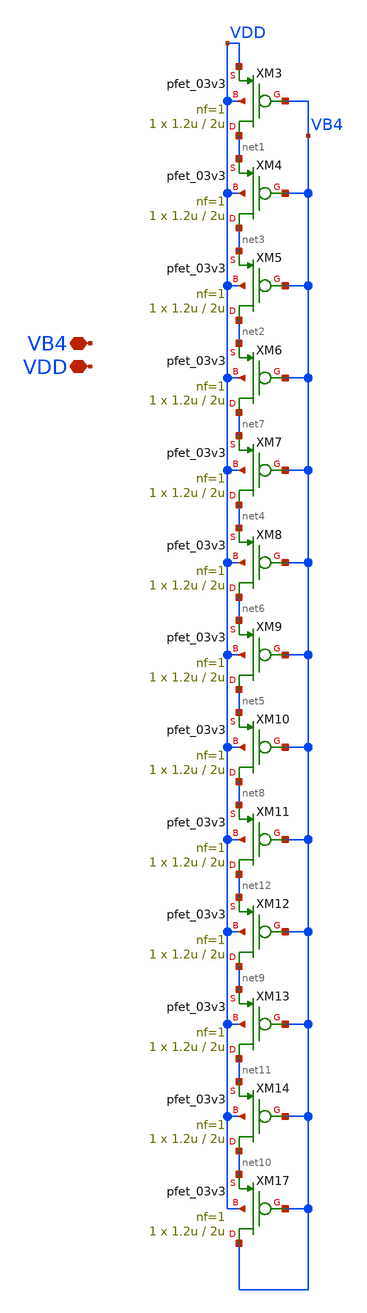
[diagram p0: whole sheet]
** sch_path: TIA_Filter/Folded/FC_bias_vb4.sch
**.subckt FC_bias_vb4 VDD VB4
*.iopin VDD
*.iopin VB4
XM3 net1 VB4 VDD VDD pfet_03v3 L=2u W=1.2u nf=1 ad='int((nf+1)/2) * W/nf * 0.18u' as='int((nf+2)/2) * W/nf * 0.18u'
+ pd='2*int((nf+1)/2) * (W/nf + 0.18u)' ps='2*int((nf+2)/2) * (W/nf + 0.18u)' nrd='0.18u / W' nrs='0.18u / W'
+ sa=0 sb=0 sd=0 m=1
XM4 net3 VB4 net1 VDD pfet_03v3 L=2u W=1.2u nf=1 ad='int((nf+1)/2) * W/nf * 0.18u' as='int((nf+2)/2) * W/nf * 0.18u'
+ pd='2*int((nf+1)/2) * (W/nf + 0.18u)' ps='2*int((nf+2)/2) * (W/nf + 0.18u)' nrd='0.18u / W' nrs='0.18u / W'
+ sa=0 sb=0 sd=0 m=1
XM5 net2 VB4 net3 VDD pfet_03v3 L=2u W=1.2u nf=1 ad='int((nf+1)/2) * W/nf * 0.18u' as='int((nf+2)/2) * W/nf * 0.18u'
+ pd='2*int((nf+1)/2) * (W/nf + 0.18u)' ps='2*int((nf+2)/2) * (W/nf + 0.18u)' nrd='0.18u / W' nrs='0.18u / W'
+ sa=0 sb=0 sd=0 m=1
XM6 net7 VB4 net2 VDD pfet_03v3 L=2u W=1.2u nf=1 ad='int((nf+1)/2) * W/nf * 0.18u' as='int((nf+2)/2) * W/nf * 0.18u'
+ pd='2*int((nf+1)/2) * (W/nf + 0.18u)' ps='2*int((nf+2)/2) * (W/nf + 0.18u)' nrd='0.18u / W' nrs='0.18u / W'
+ sa=0 sb=0 sd=0 m=1
XM7 net4 VB4 net7 VDD pfet_03v3 L=2u W=1.2u nf=1 ad='int((nf+1)/2) * W/nf * 0.18u' as='int((nf+2)/2) * W/nf * 0.18u'
+ pd='2*int((nf+1)/2) * (W/nf + 0.18u)' ps='2*int((nf+2)/2) * (W/nf + 0.18u)' nrd='0.18u / W' nrs='0.18u / W'
+ sa=0 sb=0 sd=0 m=1
XM8 net6 VB4 net4 VDD pfet_03v3 L=2u W=1.2u nf=1 ad='int((nf+1)/2) * W/nf * 0.18u' as='int((nf+2)/2) * W/nf * 0.18u'
+ pd='2*int((nf+1)/2) * (W/nf + 0.18u)' ps='2*int((nf+2)/2) * (W/nf + 0.18u)' nrd='0.18u / W' nrs='0.18u / W'
+ sa=0 sb=0 sd=0 m=1
XM9 net5 VB4 net6 VDD pfet_03v3 L=2u W=1.2u nf=1 ad='int((nf+1)/2) * W/nf * 0.18u' as='int((nf+2)/2) * W/nf * 0.18u'
+ pd='2*int((nf+1)/2) * (W/nf + 0.18u)' ps='2*int((nf+2)/2) * (W/nf + 0.18u)' nrd='0.18u / W' nrs='0.18u / W'
+ sa=0 sb=0 sd=0 m=1
XM10 net8 VB4 net5 VDD pfet_03v3 L=2u W=1.2u nf=1 ad='int((nf+1)/2) * W/nf * 0.18u' as='int((nf+2)/2) * W/nf * 0.18u'
+ pd='2*int((nf+1)/2) * (W/nf + 0.18u)' ps='2*int((nf+2)/2) * (W/nf + 0.18u)' nrd='0.18u / W' nrs='0.18u / W'
+ sa=0 sb=0 sd=0 m=1
XM11 net12 VB4 net8 VDD pfet_03v3 L=2u W=1.2u nf=1 ad='int((nf+1)/2) * W/nf * 0.18u' as='int((nf+2)/2) * W/nf * 0.18u'
+ pd='2*int((nf+1)/2) * (W/nf + 0.18u)' ps='2*int((nf+2)/2) * (W/nf + 0.18u)' nrd='0.18u / W' nrs='0.18u / W'
+ sa=0 sb=0 sd=0 m=1
XM12 net9 VB4 net12 VDD pfet_03v3 L=2u W=1.2u nf=1 ad='int((nf+1)/2) * W/nf * 0.18u' as='int((nf+2)/2) * W/nf * 0.18u'
+ pd='2*int((nf+1)/2) * (W/nf + 0.18u)' ps='2*int((nf+2)/2) * (W/nf + 0.18u)' nrd='0.18u / W' nrs='0.18u / W'
+ sa=0 sb=0 sd=0 m=1
XM13 net11 VB4 net9 VDD pfet_03v3 L=2u W=1.2u nf=1 ad='int((nf+1)/2) * W/nf * 0.18u' as='int((nf+2)/2) * W/nf * 0.18u'
+ pd='2*int((nf+1)/2) * (W/nf + 0.18u)' ps='2*int((nf+2)/2) * (W/nf + 0.18u)' nrd='0.18u / W' nrs='0.18u / W'
+ sa=0 sb=0 sd=0 m=1
XM14 net10 VB4 net11 VDD pfet_03v3 L=2u W=1.2u nf=1 ad='int((nf+1)/2) * W/nf * 0.18u' as='int((nf+2)/2) * W/nf * 0.18u'
+ pd='2*int((nf+1)/2) * (W/nf + 0.18u)' ps='2*int((nf+2)/2) * (W/nf + 0.18u)' nrd='0.18u / W' nrs='0.18u / W'
+ sa=0 sb=0 sd=0 m=1
XM17 VB4 VB4 net10 VDD pfet_03v3 L=2u W=1.2u nf=1 ad='int((nf+1)/2) * W/nf * 0.18u' as='int((nf+2)/2) * W/nf * 0.18u'
+ pd='2*int((nf+1)/2) * (W/nf + 0.18u)' ps='2*int((nf+2)/2) * (W/nf + 0.18u)' nrd='0.18u / W' nrs='0.18u / W'
+ sa=0 sb=0 sd=0 m=1
**.ends
.end
